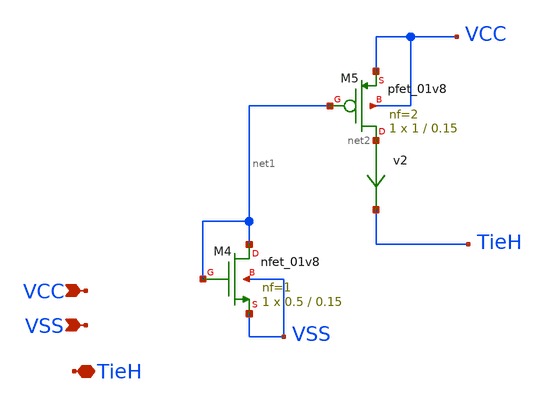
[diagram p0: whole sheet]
** sch_path: xschem_sim/TieH_1p8.sch
**.subckt TieH_1p8 VCC VSS TieH
*.ipin VCC
*.ipin VSS
*.iopin TieH
v2 net2 TieH 0
.save i(v2)
XM4 net1 net1 VSS VSS sky130_fd_pr__nfet_01v8 L=0.15 W=0.5 nf=1 ad='int((nf+1)/2) * W/nf * 0.29' as='int((nf+2)/2) * W/nf * 0.29'
+ pd='2*int((nf+1)/2) * (W/nf + 0.29)' ps='2*int((nf+2)/2) * (W/nf + 0.29)' nrd='0.29 / W' nrs='0.29 / W'
+ sa=0 sb=0 sd=0 mult=1 m=1
XM5 net2 net1 VCC VCC sky130_fd_pr__pfet_01v8 L=0.15 W=1 nf=2 ad='int((nf+1)/2) * W/nf * 0.29' as='int((nf+2)/2) * W/nf * 0.29'
+ pd='2*int((nf+1)/2) * (W/nf + 0.29)' ps='2*int((nf+2)/2) * (W/nf + 0.29)' nrd='0.29 / W' nrs='0.29 / W'
+ sa=0 sb=0 sd=0 mult=1 m=1
**.ends
.end
